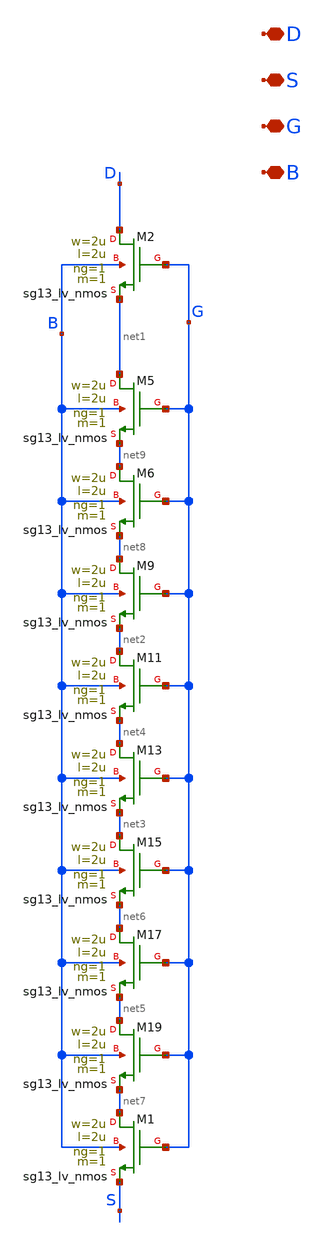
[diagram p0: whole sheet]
** sch_path: current_generator/analog/DAC/schematics/current_mirror_nmos.sch
**.subckt current_mirror_nmos D S G B
*.iopin D
*.iopin S
*.iopin G
*.iopin B
XM2 D G net1 B sg13_lv_nmos w=2u l=2u ng=1 m=1 mm_ok=1
XM5 net1 G net9 B sg13_lv_nmos w=2u l=2u ng=1 m=1 mm_ok=1
XM6 net9 G net8 B sg13_lv_nmos w=2u l=2u ng=1 m=1 mm_ok=1
XM9 net8 G net2 B sg13_lv_nmos w=2u l=2u ng=1 m=1 mm_ok=1
XM11 net2 G net4 B sg13_lv_nmos w=2u l=2u ng=1 m=1 mm_ok=1
XM13 net4 G net3 B sg13_lv_nmos w=2u l=2u ng=1 m=1 mm_ok=1
XM15 net3 G net6 B sg13_lv_nmos w=2u l=2u ng=1 m=1 mm_ok=1
XM17 net6 G net5 B sg13_lv_nmos w=2u l=2u ng=1 m=1 mm_ok=1
XM19 net5 G net7 B sg13_lv_nmos w=2u l=2u ng=1 m=1 mm_ok=1
XM1 net7 G S B sg13_lv_nmos w=2u l=2u ng=1 m=1 mm_ok=1
**.ends
.end
